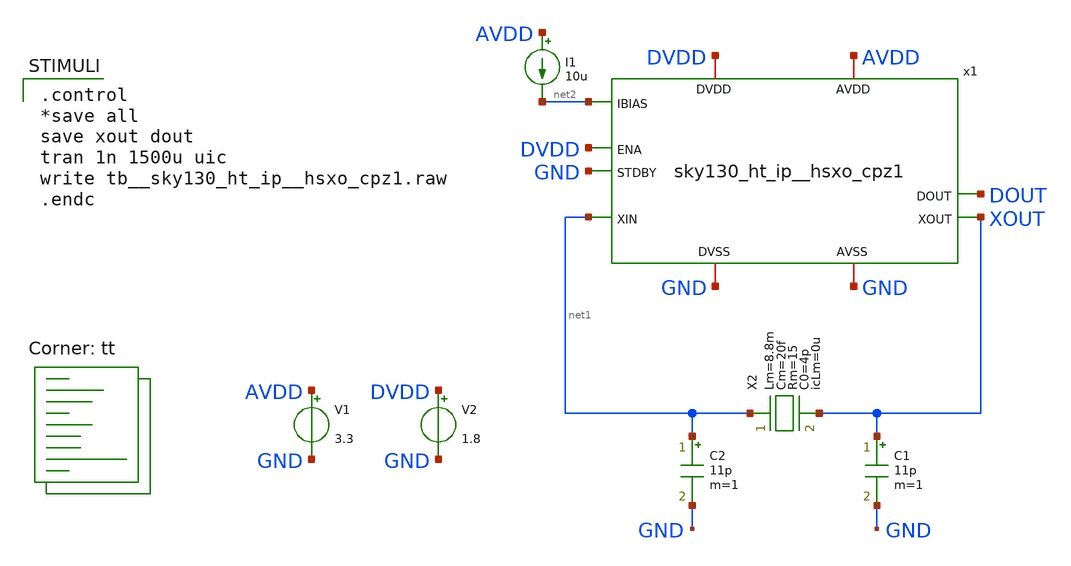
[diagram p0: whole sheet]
** sch_path: xschem/tb__sky130_ht_ip__hsxo_cpz1.sch
**.subckt tb__sky130_ht_ip__hsxo_cpz1
x1 XOUT net1 DVDD GND DOUT AVDD DVDD GND GND net2 sky130_ht_ip__hsxo_cpz1
X2 net1 XOUT crystal_model Lm=8.8m Cm=20f Rm=15 C0=4p icLm=0u
C1 XOUT GND 11p m=1
C2 net1 GND 11p m=1
I1 AVDD net2 10u
V1 AVDD GND 3.3
V2 DVDD GND 1.8
**** begin user architecture code
.lib $::SKYWATER_MODELS/sky130.lib.spice tt

.control
*save all
save xout dout
tran 1n 1500u uic
write tb__sky130_ht_ip__hsxo_cpz1.raw
.endc


**** end user architecture code
**.ends

* expanding   symbol:  /foss/designs/test5/sky130_ht_ip__hsxo_cpz1.sym # of pins=10
** sym_path: xschem/sky130_ht_ip__hsxo_cpz1.sym
** sch_path: xschem/sky130_ht_ip__hsxo_cpz1.sch
.subckt sky130_ht_ip__hsxo_cpz1 XOUT XIN ENA STDBY DOUT AVDD DVDD AVSS DVSS IBIAS
*.iopin DVDD
*.iopin DVSS
*.iopin AVDD
*.iopin AVSS
*.ipin ENA
*.ipin STDBY
*.ipin XIN
*.opin XOUT
*.opin DOUT
*.ipin IBIAS
x1 XOUT net2 net1 XIN net3 AOUT net6 net5 vittoz_pierce_osc
x2 net4 AIN DOUT net7 schmitt_trigger_pullmid
x3 AVDD ENA_B DVDD ENA ENA_H AVSS DVSS ENA_BH level_shifter
x4 AVDD STDBY_B DVDD STDBY STDBY_H AVSS DVSS STDBY_BH level_shifter
XM18 net7 STDBY_B DVSS DVSS sky130_fd_pr__nfet_01v8 L=0.15 W=8 nf=4 ad='int((nf+1)/2) * W/nf * 0.29'
+ as='int((nf+2)/2) * W/nf * 0.29' pd='2*int((nf+1)/2) * (W/nf + 0.29)' ps='2*int((nf+2)/2) * (W/nf + 0.29)'
+ nrd='0.29 / W' nrs='0.29 / W' sa=0 sb=0 sd=0 mult=1 m=1
XM21 net5 ENA_H AVSS AVSS sky130_fd_pr__nfet_g5v0d10v5 L=0.5 W=8 nf=4 ad='int((nf+1)/2) * W/nf * 0.29'
+ as='int((nf+2)/2) * W/nf * 0.29' pd='2*int((nf+1)/2) * (W/nf + 0.29)' ps='2*int((nf+2)/2) * (W/nf + 0.29)'
+ nrd='0.29 / W' nrs='0.29 / W' sa=0 sb=0 sd=0 mult=1 m=1
XM25 net1 ENA_BH AVDD AVDD sky130_fd_pr__pfet_g5v0d10v5 L=0.5 W=8 nf=4 ad='int((nf+1)/2) * W/nf * 0.29'
+ as='int((nf+2)/2) * W/nf * 0.29' pd='2*int((nf+1)/2) * (W/nf + 0.29)' ps='2*int((nf+2)/2) * (W/nf + 0.29)'
+ nrd='0.29 / W' nrs='0.29 / W' sa=0 sb=0 sd=0 mult=1 m=1
XM27 net4 STDBY DVDD DVDD sky130_fd_pr__pfet_01v8 L=0.15 W=8 nf=4 ad='int((4 + 1)/2) * 8 / 4 * 0.29'
+ as='int((4 + 2)/2) * 8 / 4 * 0.29' pd='2*int((4 + 1)/2) * (8 / 4 + 0.29)' ps='2*int((4 + 2)/2) * (8 / 4 + 0.29)'
+ nrd='0.29 / 8 ' nrs='0.29 / 8 ' sa=0 sb=0 sd=0 mult=1 m=1
XM1 net2 STDBY_H AVDD AVDD sky130_fd_pr__pfet_g5v0d10v5 L=0.5 W=8 nf=4 ad='int((nf+1)/2) * W/nf * 0.29'
+ as='int((nf+2)/2) * W/nf * 0.29' pd='2*int((nf+1)/2) * (W/nf + 0.29)' ps='2*int((nf+2)/2) * (W/nf + 0.29)'
+ nrd='0.29 / W' nrs='0.29 / W' sa=0 sb=0 sd=0 mult=1 m=1
XM2 net3 ENA_BH IBIAS AVDD sky130_fd_pr__pfet_g5v0d10v5 L=0.5 W=8 nf=4 ad='int((nf+1)/2) * W/nf * 0.29'
+ as='int((nf+2)/2) * W/nf * 0.29' pd='2*int((nf+1)/2) * (W/nf + 0.29)' ps='2*int((nf+2)/2) * (W/nf + 0.29)'
+ nrd='0.29 / W' nrs='0.29 / W' sa=0 sb=0 sd=0 mult=1 m=1
XM3 net6 STDBY_BH AVSS AVSS sky130_fd_pr__nfet_g5v0d10v5 L=0.5 W=8 nf=4 ad='int((nf+1)/2) * W/nf * 0.29'
+ as='int((nf+2)/2) * W/nf * 0.29' pd='2*int((nf+1)/2) * (W/nf + 0.29)' ps='2*int((nf+2)/2) * (W/nf + 0.29)'
+ nrd='0.29 / W' nrs='0.29 / W' sa=0 sb=0 sd=0 mult=1 m=1
XM4 DOUT STDBY DVSS DVSS sky130_fd_pr__nfet_01v8 L=0.15 W=8 nf=4 ad='int((nf+1)/2) * W/nf * 0.29' as='int((nf+2)/2) * W/nf * 0.29'
+ pd='2*int((nf+1)/2) * (W/nf + 0.29)' ps='2*int((nf+2)/2) * (W/nf + 0.29)' nrd='0.29 / W' nrs='0.29 / W'
+ sa=0 sb=0 sd=0 mult=1 m=1
XC3 AVDD AVSS sky130_fd_pr__cap_mim_m3_1 W=15 L=15 MF=6 m=6
XC4 DVDD DVSS sky130_fd_pr__cap_mim_m3_1 W=15 L=15 MF=6 m=6
XD1 XIN AVDD sky130_fd_pr__diode_pw2nd_05v5 area=2e11 pj=1.8e6
XD2 AVSS XIN sky130_fd_pr__diode_pw2nd_05v5 area=2e11 pj=1.8e6
XC1 AOUT AIN sky130_fd_pr__cap_mim_m3_1 W=15 L=15 MF=6 m=6
.ends


* expanding   symbol:  /foss/designs/test5/crystal_model.sym # of pins=2
** sym_path: xschem/crystal_model.sym
** sch_path: xschem/crystal_model.sch
.subckt crystal_model XIN XOUT  Lm=8.8m Cm=20f Rm=15 C0=4p icLm=0m
*.iopin XIN
*.iopin XOUT
Cm net1 net2 C=Cm m=1
Lm XIN net1 L=Lm ic=icLm m=1
Rm net2 XOUT R=Rm m=1
C0 XIN XOUT C=C0 m=1
.ends


* expanding   symbol:  /foss/designs/test5/vittoz_pierce_osc.sym # of pins=8
** sym_path: xschem/vittoz_pierce_osc.sym
** sch_path: xschem/vittoz_pierce_osc.sch
.subckt vittoz_pierce_osc XOUT SG_AVDD EG_AVDD XIN IBIAS AOUT SG_AVSS EG_AVSS
*.iopin EG_AVDD
*.iopin EG_AVSS
*.iopin SG_AVDD
*.iopin SG_AVSS
*.ipin XIN
*.ipin IBIAS
*.opin XOUT
*.opin AOUT
XM9 net6 PBIAS EG_AVDD EG_AVDD sky130_fd_pr__pfet_g5v0d10v5 L=0.5 W=1024 nf=32 ad='int((nf+1)/2) * W/nf * 0.29'
+ as='int((nf+2)/2) * W/nf * 0.29' pd='2*int((nf+1)/2) * (W/nf + 0.29)' ps='2*int((nf+2)/2) * (W/nf + 0.29)'
+ nrd='0.29 / W' nrs='0.29 / W' sa=0 sb=0 sd=0 mult=1 m=1
XM10 net7 PBIAS EG_AVDD EG_AVDD sky130_fd_pr__pfet_g5v0d10v5 L=0.5 W=128 nf=4 ad='int((nf+1)/2) * W/nf * 0.29'
+ as='int((nf+2)/2) * W/nf * 0.29' pd='2*int((nf+1)/2) * (W/nf + 0.29)' ps='2*int((nf+2)/2) * (W/nf + 0.29)'
+ nrd='0.29 / W' nrs='0.29 / W' sa=0 sb=0 sd=0 mult=1 m=1
XM11 PBIAS PBIAS EG_AVDD EG_AVDD sky130_fd_pr__pfet_g5v0d10v5 L=0.5 W=128 nf=4 ad='int((nf+1)/2) * W/nf * 0.29'
+ as='int((nf+2)/2) * W/nf * 0.29' pd='2*int((nf+1)/2) * (W/nf + 0.29)' ps='2*int((nf+2)/2) * (W/nf + 0.29)'
+ nrd='0.29 / W' nrs='0.29 / W' sa=0 sb=0 sd=0 mult=1 m=1
Vmeas5 net6 XOUT 0
.save i(vmeas5)
Vmeas6 net7 net1 0
.save i(vmeas6)
Vmeas7 PBIAS net3 0
.save i(vmeas7)
XM12 net1 net2 EG_AVSS EG_AVSS sky130_fd_pr__nfet_g5v0d10v5 L=0.5 W=128 nf=4 ad='int((nf+1)/2) * W/nf * 0.29'
+ as='int((nf+2)/2) * W/nf * 0.29' pd='2*int((nf+1)/2) * (W/nf + 0.29)' ps='2*int((nf+2)/2) * (W/nf + 0.29)'
+ nrd='0.29 / W' nrs='0.29 / W' sa=0 sb=0 sd=0 mult=1 m=1
XR1 net2 net1 EG_AVSS sky130_fd_pr__res_xhigh_po_0p35 L=7 mult=1 m=1
XC1 net1 EG_AVSS sky130_fd_pr__cap_mim_m3_1 W=1 L=1 MF=1 m=1
XC2 XIN net2 sky130_fd_pr__cap_mim_m3_1 W=15 L=15 MF=6 m=6
XC7 net2 EG_AVSS sky130_fd_pr__cap_mim_m3_1 W=15 L=15 MF=6 m=6
XM13 XOUT XIN EG_AVSS EG_AVSS sky130_fd_pr__nfet_g5v0d10v5 L=0.5 W=32 nf=8 ad='int((nf+1)/2) * W/nf * 0.29'
+ as='int((nf+2)/2) * W/nf * 0.29' pd='2*int((nf+1)/2) * (W/nf + 0.29)' ps='2*int((nf+2)/2) * (W/nf + 0.29)'
+ nrd='0.29 / W' nrs='0.29 / W' sa=0 sb=0 sd=0 mult=1 m=1
XM14 net3 net2 net5 EG_AVSS sky130_fd_pr__nfet_g5v0d10v5 L=0.5 W=1024 nf=32 ad='int((nf+1)/2) * W/nf * 0.29'
+ as='int((nf+2)/2) * W/nf * 0.29' pd='2*int((nf+1)/2) * (W/nf + 0.29)' ps='2*int((nf+2)/2) * (W/nf + 0.29)'
+ nrd='0.29 / W' nrs='0.29 / W' sa=0 sb=0 sd=0 mult=1 m=1
XM15 net5 net4 EG_AVSS EG_AVSS sky130_fd_pr__nfet_g5v0d10v5 L=0.5 W=128 nf=4 ad='int((nf+1)/2) * W/nf * 0.29'
+ as='int((nf+2)/2) * W/nf * 0.29' pd='2*int((nf+1)/2) * (W/nf + 0.29)' ps='2*int((nf+2)/2) * (W/nf + 0.29)'
+ nrd='0.29 / W' nrs='0.29 / W' sa=0 sb=0 sd=0 mult=1 m=1
XM16 net4 net4 EG_AVSS EG_AVSS sky130_fd_pr__nfet_g5v0d10v5 L=0.5 W=128 nf=4 ad='int((nf+1)/2) * W/nf * 0.29'
+ as='int((nf+2)/2) * W/nf * 0.29' pd='2*int((nf+1)/2) * (W/nf + 0.29)' ps='2*int((nf+2)/2) * (W/nf + 0.29)'
+ nrd='0.29 / W' nrs='0.29 / W' sa=0 sb=0 sd=0 mult=1 m=1
XR3 XIN XOUT EG_AVSS sky130_fd_pr__res_xhigh_po_0p35 L=2.8 mult=1 m=1
XM17 AOUT XIN SG_AVSS SG_AVSS sky130_fd_pr__nfet_g5v0d10v5 L=0.5 W=4 nf=1 ad='int((nf+1)/2) * W/nf * 0.29'
+ as='int((nf+2)/2) * W/nf * 0.29' pd='2*int((nf+1)/2) * (W/nf + 0.29)' ps='2*int((nf+2)/2) * (W/nf + 0.29)'
+ nrd='0.29 / W' nrs='0.29 / W' sa=0 sb=0 sd=0 mult=1 m=1
XM18 net8 PBIAS SG_AVDD SG_AVDD sky130_fd_pr__pfet_g5v0d10v5 L=0.5 W=128 nf=4 ad='int((nf+1)/2) * W/nf * 0.29'
+ as='int((nf+2)/2) * W/nf * 0.29' pd='2*int((nf+1)/2) * (W/nf + 0.29)' ps='2*int((nf+2)/2) * (W/nf + 0.29)'
+ nrd='0.29 / W' nrs='0.29 / W' sa=0 sb=0 sd=0 mult=1 m=1
Vmeas8 net8 AOUT 0
.save i(vmeas8)
XC8 AOUT SG_AVSS sky130_fd_pr__cap_mim_m3_1 W=0.5 L=0.5 MF=12 m=12
XC3 EG_AVDD EG_AVSS sky130_fd_pr__cap_mim_m3_1 W=15 L=15 MF=6 m=6
XC4 SG_AVDD SG_AVSS sky130_fd_pr__cap_mim_m3_1 W=15 L=15 MF=6 m=6
Vmeas1 IBIAS net4 0
.save i(vmeas1)
.ends


* expanding   symbol:  /foss/designs/test5/schmitt_trigger_pullmid.sym # of pins=4
** sym_path: xschem/schmitt_trigger_pullmid.sym
** sch_path: xschem/schmitt_trigger_pullmid.sch
.subckt schmitt_trigger_pullmid SG_DVDD AIN DOUT SG_DVSS
*.iopin SG_DVDD
*.iopin SG_DVSS
*.ipin AIN
*.opin DOUT
XM1 DMID DMID SG_DVDD SG_DVDD sky130_fd_pr__pfet_01v8 L=6 W=0.5 nf=1 ad='int((1 + 1)/2) * 0.5 / 1 * 0.29'
+ as='int((1 + 2)/2) * 0.5 / 1 * 0.29' pd='2*int((1 + 1)/2) * (0.5 / 1 + 0.29)' ps='2*int((1 + 2)/2) * (0.5 / 1 + 0.29)'
+ nrd='0.29 / 0.5 ' nrs='0.29 / 0.5 ' sa=0 sb=0 sd=0 mult=1 m=1
XM2 DMID DMID SG_DVSS SG_DVSS sky130_fd_pr__nfet_01v8 L=4 W=0.5 nf=1 ad='int((nf+1)/2) * W/nf * 0.29'
+ as='int((nf+2)/2) * W/nf * 0.29' pd='2*int((nf+1)/2) * (W/nf + 0.29)' ps='2*int((nf+2)/2) * (W/nf + 0.29)'
+ nrd='0.29 / W' nrs='0.29 / W' sa=0 sb=0 sd=0 mult=1 m=1
XR2 AIN DMID SG_DVSS sky130_fd_pr__res_xhigh_po_0p35 L=128 mult=1 m=1
XM3 DOUT AIN DHT SG_DVDD sky130_fd_pr__pfet_01v8 L=0.3 W=1 nf=1 ad='int((1 + 1)/2) * 1 / 1 * 0.29' as='int((1 + 2)/2) * 1 / 1 * 0.29'
+ pd='2*int((1 + 1)/2) * (1 / 1 + 0.29)' ps='2*int((1 + 2)/2) * (1 / 1 + 0.29)' nrd='0.29 / 1 ' nrs='0.29 / 1 '
+ sa=0 sb=0 sd=0 mult=1 m=1
XM4 DOUT AIN DLT SG_DVSS sky130_fd_pr__nfet_01v8 L=0.2 W=1 nf=1 ad='int((nf+1)/2) * W/nf * 0.29' as='int((nf+2)/2) * W/nf * 0.29'
+ pd='2*int((nf+1)/2) * (W/nf + 0.29)' ps='2*int((nf+2)/2) * (W/nf + 0.29)' nrd='0.29 / W' nrs='0.29 / W'
+ sa=0 sb=0 sd=0 mult=1 m=1
XM5 DHT AIN SG_DVDD SG_DVDD sky130_fd_pr__pfet_01v8 L=0.3 W=1 nf=1 ad='int((1 + 1)/2) * 1 / 1 * 0.29'
+ as='int((1 + 2)/2) * 1 / 1 * 0.29' pd='2*int((1 + 1)/2) * (1 / 1 + 0.29)' ps='2*int((1 + 2)/2) * (1 / 1 + 0.29)'
+ nrd='0.29 / 1 ' nrs='0.29 / 1 ' sa=0 sb=0 sd=0 mult=1 m=1
XM6 DLT AIN SG_DVSS SG_DVSS sky130_fd_pr__nfet_01v8 L=0.2 W=1 nf=1 ad='int((nf+1)/2) * W/nf * 0.29' as='int((nf+2)/2) * W/nf * 0.29'
+ pd='2*int((nf+1)/2) * (W/nf + 0.29)' ps='2*int((nf+2)/2) * (W/nf + 0.29)' nrd='0.29 / W' nrs='0.29 / W'
+ sa=0 sb=0 sd=0 mult=1 m=1
XM7 SG_DVSS DOUT DHT SG_DVDD sky130_fd_pr__pfet_01v8 L=0.3 W=1 nf=1 ad='int((1 + 1)/2) * 1 / 1 * 0.29'
+ as='int((1 + 2)/2) * 1 / 1 * 0.29' pd='2*int((1 + 1)/2) * (1 / 1 + 0.29)' ps='2*int((1 + 2)/2) * (1 / 1 + 0.29)'
+ nrd='0.29 / 1 ' nrs='0.29 / 1 ' sa=0 sb=0 sd=0 mult=1 m=1
XM8 SG_DVDD DOUT DLT SG_DVSS sky130_fd_pr__nfet_01v8 L=0.2 W=1 nf=1 ad='int((nf+1)/2) * W/nf * 0.29'
+ as='int((nf+2)/2) * W/nf * 0.29' pd='2*int((nf+1)/2) * (W/nf + 0.29)' ps='2*int((nf+2)/2) * (W/nf + 0.29)'
+ nrd='0.29 / W' nrs='0.29 / W' sa=0 sb=0 sd=0 mult=1 m=1
XC4 SG_DVDD SG_DVSS sky130_fd_pr__cap_mim_m3_1 W=15 L=15 MF=6 m=6
.ends


* expanding   symbol:  /foss/designs/test5/level_shifter.sym # of pins=8
** sym_path: xschem/level_shifter.sym
** sch_path: xschem/level_shifter.sch
.subckt level_shifter AVDD LO_B DVDD LO HI AVSS DVSS HI_B
*.iopin DVDD
*.iopin DVSS
*.iopin AVDD
*.iopin AVSS
*.ipin LO
*.opin LO_B
*.opin HI
*.opin HI_B
XM18 LO_B LO DVSS DVSS sky130_fd_pr__nfet_01v8 L=0.15 W=1 nf=1 ad='int((nf+1)/2) * W/nf * 0.29' as='int((nf+2)/2) * W/nf * 0.29'
+ pd='2*int((nf+1)/2) * (W/nf + 0.29)' ps='2*int((nf+2)/2) * (W/nf + 0.29)' nrd='0.29 / W' nrs='0.29 / W'
+ sa=0 sb=0 sd=0 mult=1 m=1
XM21 HI_B LO AVSS AVSS sky130_fd_pr__nfet_g5v0d10v5 L=0.5 W=1 nf=1 ad='int((nf+1)/2) * W/nf * 0.29' as='int((nf+2)/2) * W/nf * 0.29'
+ pd='2*int((nf+1)/2) * (W/nf + 0.29)' ps='2*int((nf+2)/2) * (W/nf + 0.29)' nrd='0.29 / W' nrs='0.29 / W'
+ sa=0 sb=0 sd=0 mult=1 m=1
XM25 HI_B HI AVDD AVDD sky130_fd_pr__pfet_g5v0d10v5 L=0.5 W=1 nf=1 ad='int((nf+1)/2) * W/nf * 0.29' as='int((nf+2)/2) * W/nf * 0.29'
+ pd='2*int((nf+1)/2) * (W/nf + 0.29)' ps='2*int((nf+2)/2) * (W/nf + 0.29)' nrd='0.29 / W' nrs='0.29 / W'
+ sa=0 sb=0 sd=0 mult=1 m=1
XM27 LO_B LO DVDD DVDD sky130_fd_pr__pfet_01v8 L=0.15 W=1 nf=1 ad='int((1 + 1)/2) * 1 / 1 * 0.29' as='int((1 + 2)/2) * 1 / 1 * 0.29'
+ pd='2*int((1 + 1)/2) * (1 / 1 + 0.29)' ps='2*int((1 + 2)/2) * (1 / 1 + 0.29)' nrd='0.29 / 1 ' nrs='0.29 / 1 '
+ sa=0 sb=0 sd=0 mult=1 m=1
XM1 HI HI_B AVDD AVDD sky130_fd_pr__pfet_g5v0d10v5 L=0.5 W=1 nf=1 ad='int((nf+1)/2) * W/nf * 0.29' as='int((nf+2)/2) * W/nf * 0.29'
+ pd='2*int((nf+1)/2) * (W/nf + 0.29)' ps='2*int((nf+2)/2) * (W/nf + 0.29)' nrd='0.29 / W' nrs='0.29 / W'
+ sa=0 sb=0 sd=0 mult=1 m=1
XM2 HI LO_B AVSS AVSS sky130_fd_pr__nfet_g5v0d10v5 L=0.5 W=1 nf=1 ad='int((nf+1)/2) * W/nf * 0.29' as='int((nf+2)/2) * W/nf * 0.29'
+ pd='2*int((nf+1)/2) * (W/nf + 0.29)' ps='2*int((nf+2)/2) * (W/nf + 0.29)' nrd='0.29 / W' nrs='0.29 / W'
+ sa=0 sb=0 sd=0 mult=1 m=1
.ends

.end
